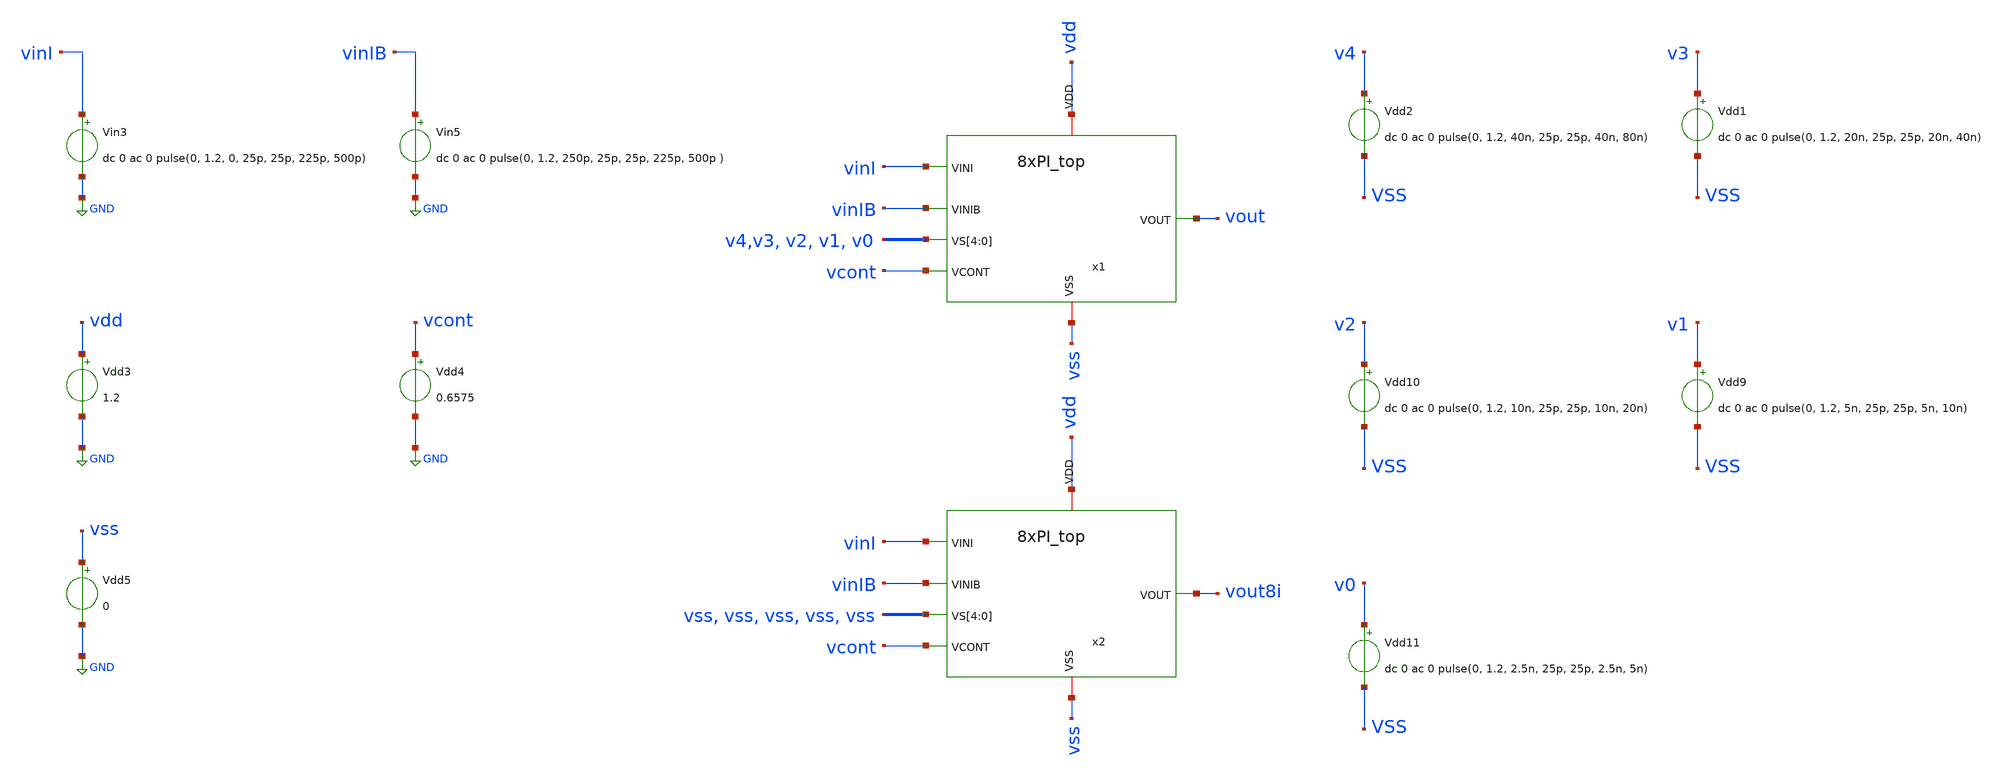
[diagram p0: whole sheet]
** sch_path: 8xPI_top/tb_8xpi_linearity_integration.sch
**.subckt tb_8xpi_linearity_integration
x1 vdd v4 v3 v2 v1 v0 vinI vinIB vout vcont vss 8xPI_top
Vin3 vinI GND dc 0 ac 0 pulse(0, 1.2, 0, 25p, 25p, 225p, 500p)
Vin5 vinIB GND dc 0 ac 0 pulse(0, 1.2, 250p, 25p, 25p, 225p, 500p )
x2 vdd vss vss vss vss vss vinI vinIB vout8i vcont vss 8xPI_top
Vdd9 v1 VSS dc 0 ac 0 pulse(0, 1.2, 5n, 25p, 25p, 5n, 10n)
Vdd10 v2 VSS dc 0 ac 0 pulse(0, 1.2, 10n, 25p, 25p, 10n, 20n)
Vdd11 v0 VSS dc 0 ac 0 pulse(0, 1.2, 2.5n, 25p, 25p, 2.5n, 5n)
Vdd1 v3 VSS dc 0 ac 0 pulse(0, 1.2, 20n, 25p, 25p, 20n, 40n)
Vdd2 v4 VSS dc 0 ac 0 pulse(0, 1.2, 40n, 25p, 25p, 40n, 80n)
Vdd3 vdd GND 1.2
Vdd4 vcont GND 0.6575
Vdd5 vss GND 0
**** begin user architecture code



* Circuit Parameters
.param vdd = 1.2
.param vss = 0.0
.param a=0
.param b=0
.param c=0
.param d=1
.param Tclk = 500P
.options TEMP = 27.0

* Include Models
*.lib /opt/pdks/ihp-sg13g2/libs.tech/ngspice/models/cornerMOSlv.lib mos_tt
*.lib /opt/pdks/ihp-sg13g2/libs.tech/ngspice/models/cornerMOShv.lib mos_tt
*.lib /opt/pdks/ihp-sg13g2/libs.tech/ngspice/models/cornerHBT.lib hbt_typ
*.lib /opt/pdks/ihp-sg13g2/libs.tech/ngspice/models/cornerRES.lib res_typ
.lib cornerMOSlv.lib mos_tt


* OP Parameters & Singals to save
.save V(vout) V(vout8i) V(vinI) V(vinIB) V(x1.vsq[2]) V(x1.vsq[1]) V(x1.vsq[0]) V(x1.vst[7]) V(x1.vst[6]) V(x1.vst[5]) V(x1.vst[4]) V(x1.vst[3]) V(x1.vst[2]) V(x1.vst[1]) V(x1.vstq[7]) V(x1.vstq[6]) V(x1.vstq[5]) V(x1.vstq[4]) V(x1.vstq[3]) V(x1.vstq[2]) V(x1.vstq[1]) V(x1.vi) V(x1.vib) V(x1.vq) V(x1.vqb)

*Simulations
.control
*set output_path = tb_linearity_8xpi/
	tran 5PS 80NS
	*setplot tran1
	*plot v0 v1+1.5 v0_st+3 v6_st+4.5 Vout+6 Vout8I+7.5 ylabel vout xlabel vin
	display
	set filetype = ascii
        write tran_linearity_integration.raw
	*V(vout) V(vout8i) V(vinI) V(vinIB) V(@x1.vsq[2]) V(x1.vst[7]) V(x1.vstq[7]) V(x1.x1.vini)
+ V(x1.x1.vinib) V(x1.x1.vinq) V(x1.x1.vinqb)
	*write {$output_path}tran_linearity_termoless.raw V(Vout) V(Vout8I) V(vinI) V(VoutI1) V(VoutI2) V(VoutQ1)
+ V(VoutIB1) V(VoutQB1)
.endc
.end

**** end user architecture code
**.ends
.GLOBAL GND
.end
